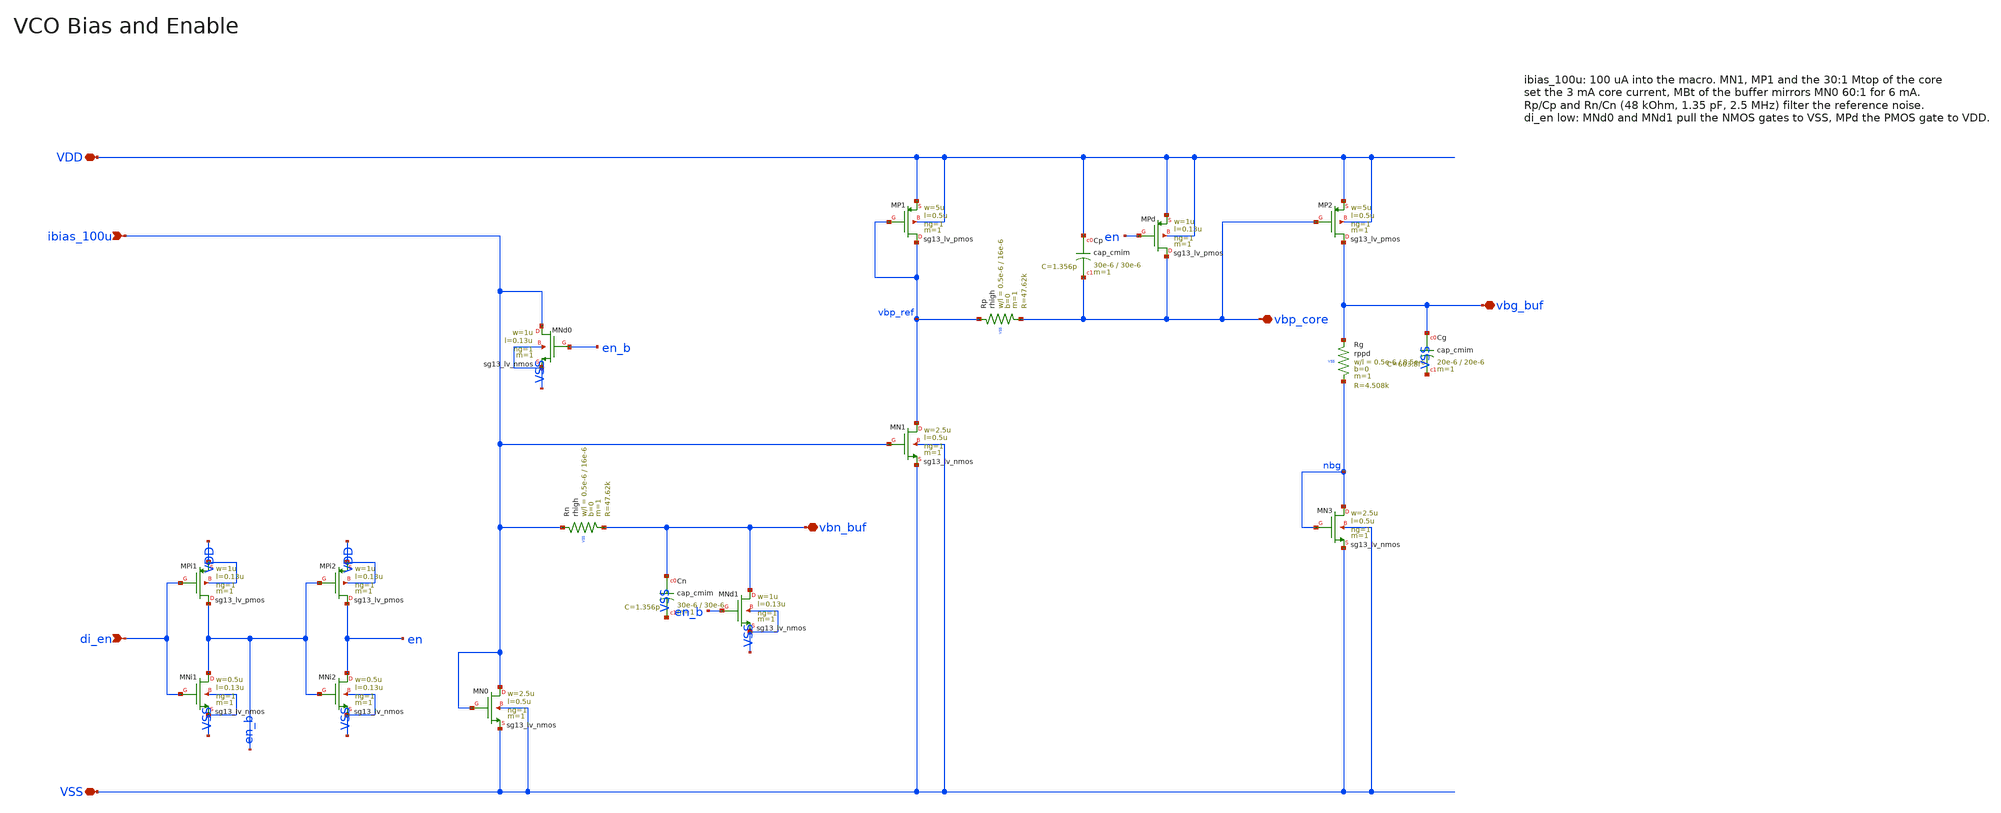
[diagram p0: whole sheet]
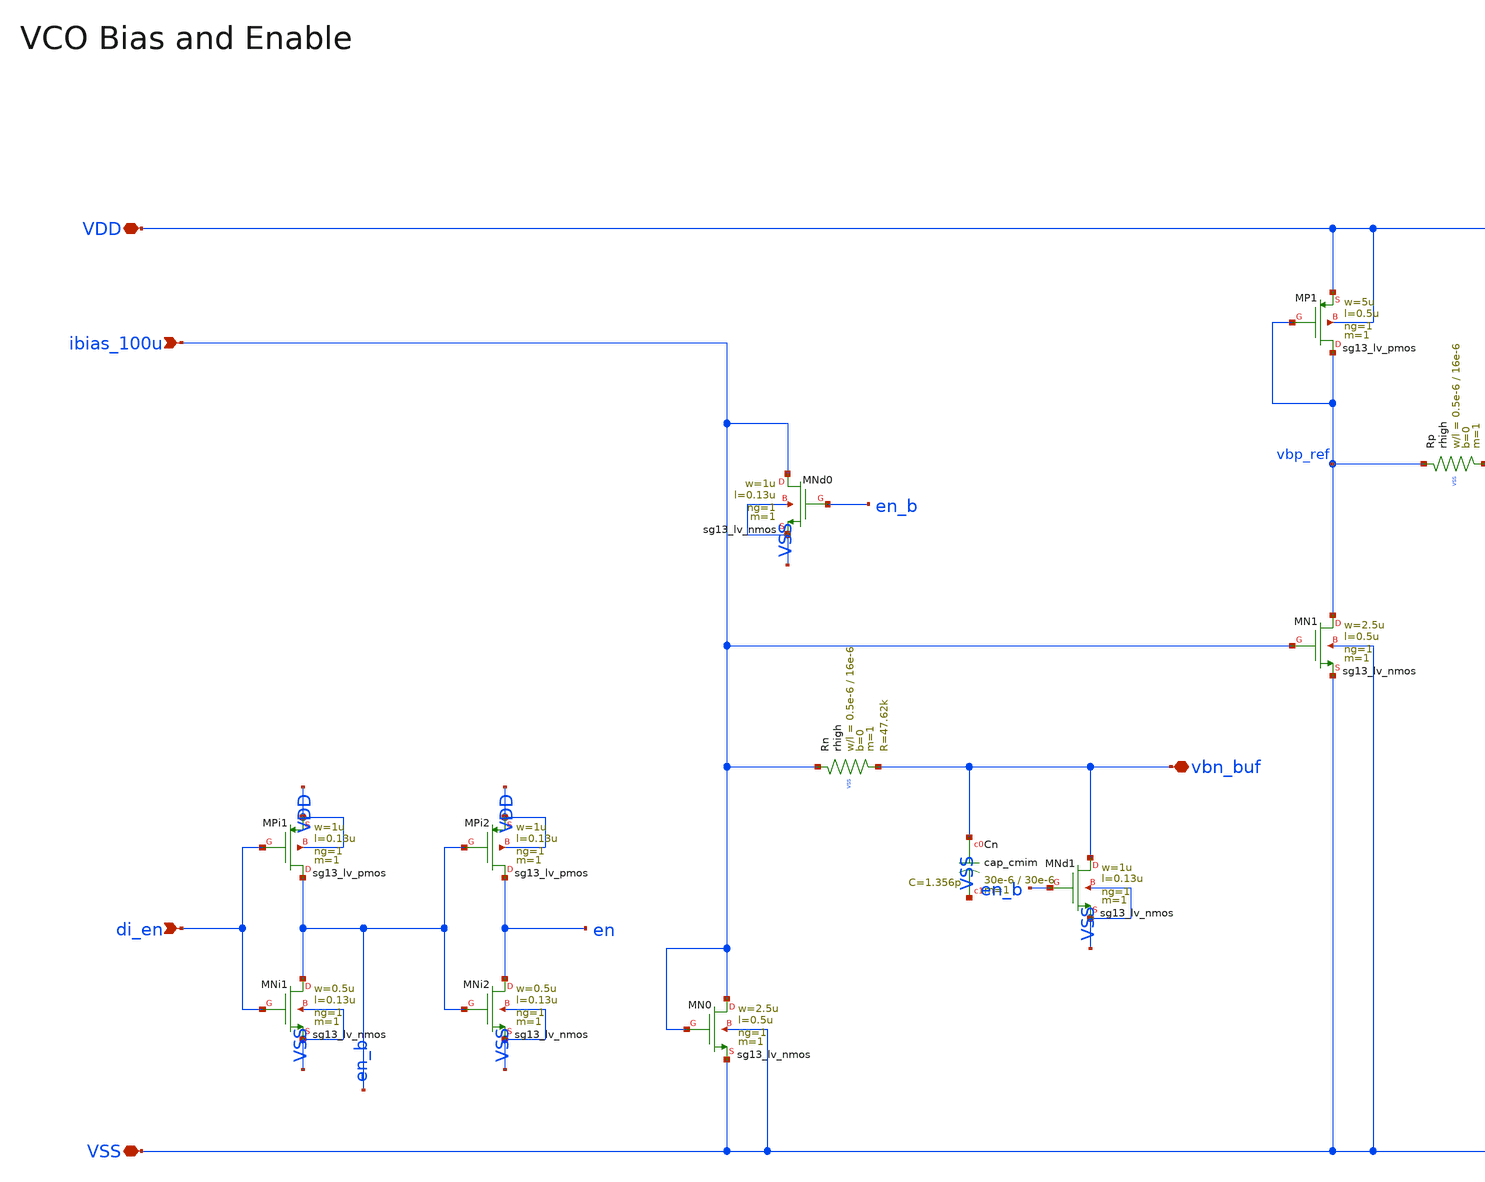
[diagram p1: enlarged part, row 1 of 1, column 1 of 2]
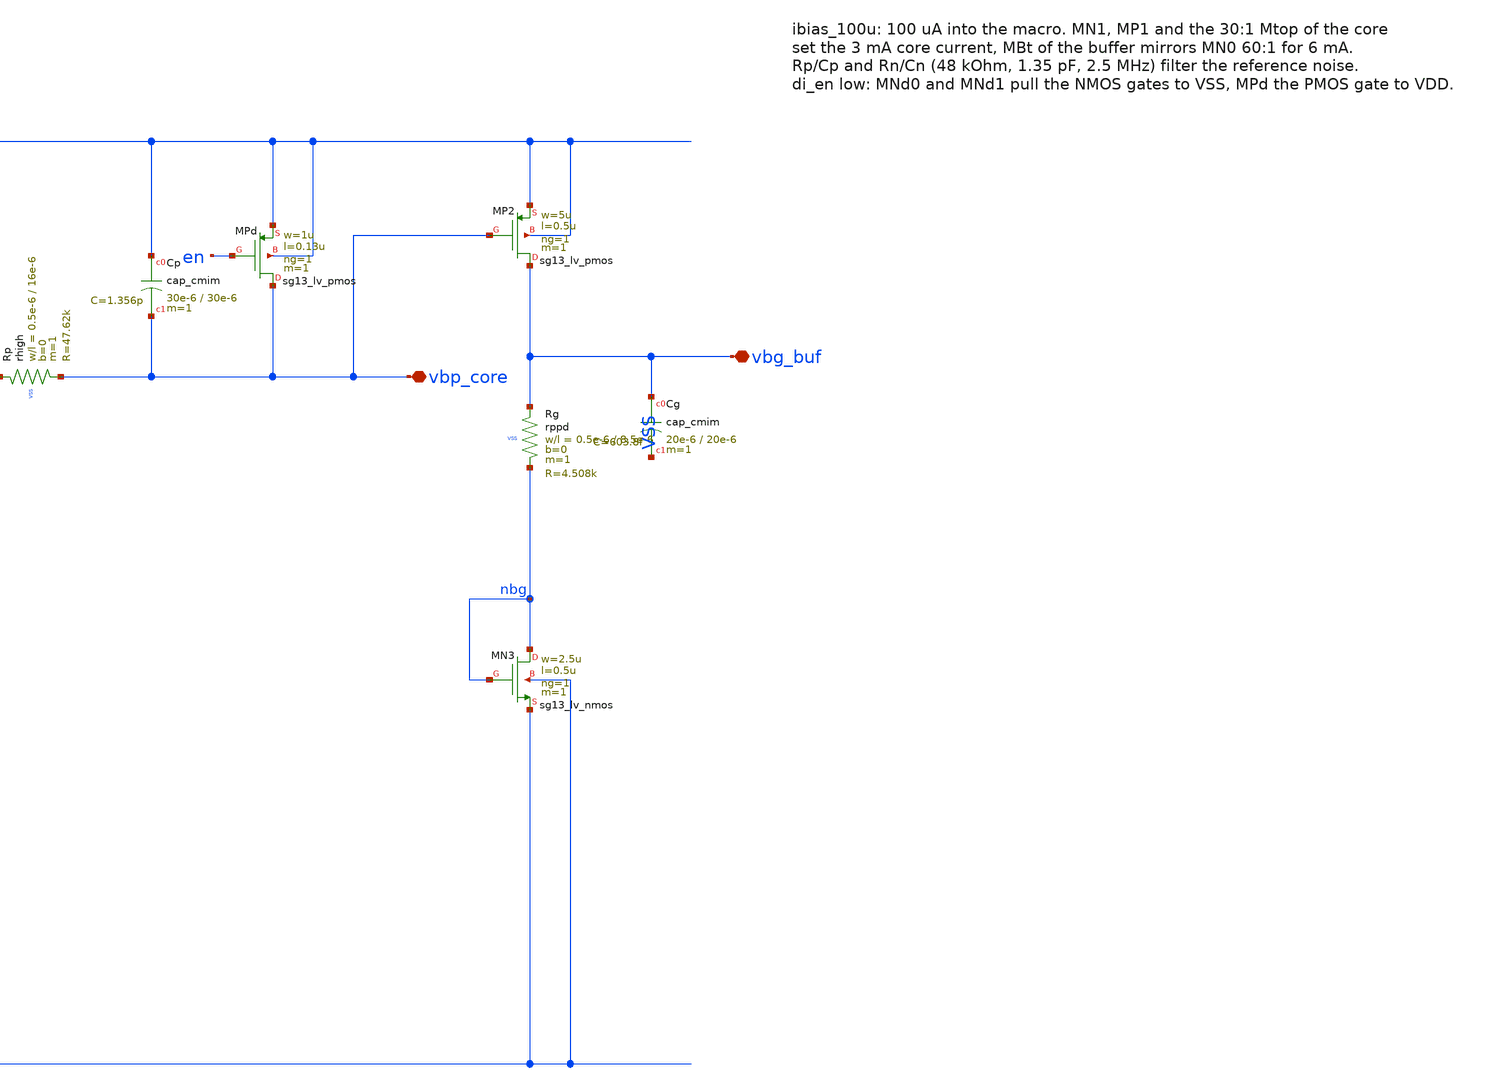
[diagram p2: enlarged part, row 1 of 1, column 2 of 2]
** sch_path: macros/vco/schematic/xschem/vco_bias.sch
**.subckt vco_bias VDD VSS di_en ibias_100u vbn_buf vbp_core vbg_buf
*.iopin VDD
*.iopin VSS
*.ipin di_en
*.ipin ibias_100u
*.iopin vbn_buf
*.iopin vbp_core
*.iopin vbg_buf
XMPi1 en_b di_en VDD VDD sg13_lv_pmos w=1u l=0.13u ng=1 m=1 mm_ok=1
XMNi1 en_b di_en VSS VSS sg13_lv_nmos w=0.5u l=0.13u ng=1 m=1 mm_ok=1
XMPi2 en en_b VDD VDD sg13_lv_pmos w=1u l=0.13u ng=1 m=1 mm_ok=1
XMNi2 en en_b VSS VSS sg13_lv_nmos w=0.5u l=0.13u ng=1 m=1 mm_ok=1
XMN0 ibias_100u ibias_100u VSS VSS sg13_lv_nmos w=2.5u l=0.5u ng=1 m=1 mm_ok=1
XMNd0 ibias_100u en_b VSS VSS sg13_lv_nmos w=1u l=0.13u ng=1 m=1 mm_ok=1
XRn ibias_100u vbn_buf VSS rhigh w=0.5e-6 l=16e-6 m=1 b=0 mm_ok=1
XCn vbn_buf VSS cap_cmim w=30e-6 l=30e-6 m=1 mm_ok=1
XMNd1 vbn_buf en_b VSS VSS sg13_lv_nmos w=1u l=0.13u ng=1 m=1 mm_ok=1
XMN1 vbp_ref ibias_100u VSS VSS sg13_lv_nmos w=2.5u l=0.5u ng=1 m=1 mm_ok=1
XMP1 vbp_ref vbp_ref VDD VDD sg13_lv_pmos w=5u l=0.5u ng=1 m=1 mm_ok=1
XRp vbp_ref vbp_core VSS rhigh w=0.5e-6 l=16e-6 m=1 b=0 mm_ok=1
XCp VDD vbp_core cap_cmim w=30e-6 l=30e-6 m=1 mm_ok=1
XMPd vbp_core en VDD VDD sg13_lv_pmos w=1u l=0.13u ng=1 m=1 mm_ok=1
XMP2 vbg_buf vbp_core VDD VDD sg13_lv_pmos w=5u l=0.5u ng=1 m=1 mm_ok=1
XRg vbg_buf nbg VSS rppd w=0.5e-6 l=8.5e-6 m=1 b=0 mm_ok=1
XMN3 nbg nbg VSS VSS sg13_lv_nmos w=2.5u l=0.5u ng=1 m=1 mm_ok=1
XCg vbg_buf VSS cap_cmim w=20e-6 l=20e-6 m=1 mm_ok=1
**.ends
.end
